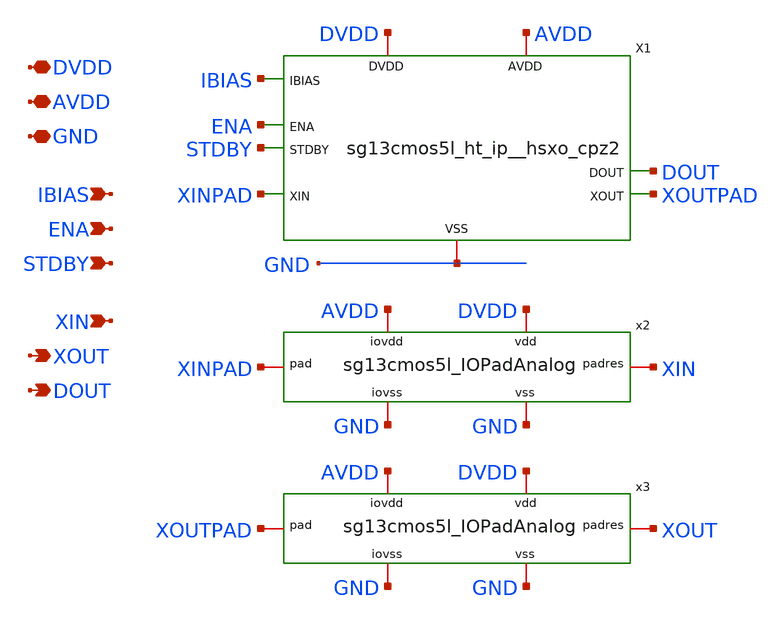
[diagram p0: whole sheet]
** sch_path: xschem/dut_with_package_v1.sch
**.subckt dut_with_package_v1 DVDD GND AVDD ENA STDBY XIN XOUT DOUT IBIAS
*.iopin DVDD
*.iopin GND
*.iopin AVDD
*.ipin ENA
*.ipin STDBY
*.ipin XIN
*.opin XOUT
*.opin DOUT
*.ipin IBIAS
X1 XOUTPAD XINPAD ENA STDBY DOUT AVDD DVDD GND IBIAS sg13cmos5l_ht_ip__hsxo_cpz2
x2 XINPAD XIN DVDD GND AVDD GND sg13cmos5l_IOPadAnalog
x3 XOUTPAD XOUT DVDD GND AVDD GND sg13cmos5l_IOPadAnalog
**.ends
.end
